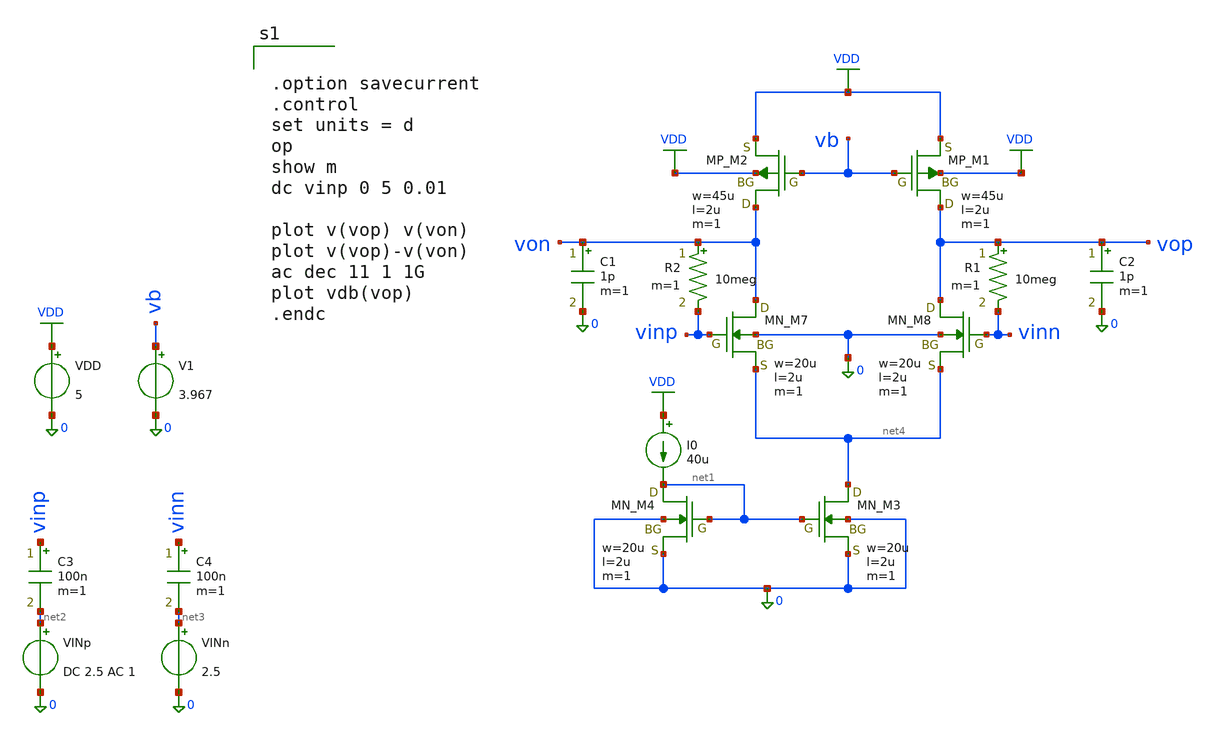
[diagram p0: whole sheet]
** sch_path: member_project/JJY_Receiver/Masahiro/jjy_recv/diff_amp/diff_amp_nin.sch
**.subckt diff_amp_nin
VDD VDD 0 5
VINp net2 0 DC 2.5 AC 1
I0 VDD net1 40u
C1 von 0 1p m=1
V1 vb 0 3.967
XM1 vop vb VDD VDD PMOS w=45u l=2u as=0 ad=0 ps=0 pd=0 nrd=0 nrs=0 m=1
XM2 von vb VDD VDD PMOS w=45u l=2u as=0 ad=0 ps=0 pd=0 nrd=0 nrs=0 m=1
XM3 net4 net1 0 0 NMOS w=20u l=2u as=0 ad=0 ps=0 pd=0 nrd=0 nrs=0 m=1
XM4 net1 net1 0 0 NMOS w=20u l=2u as=0 ad=0 ps=0 pd=0 nrd=0 nrs=0 m=1
C2 vop 0 1p m=1
VINn net3 0 2.5
XM7 von vinp net4 0 NMOS w=20u l=2u as=0 ad=0 ps=0 pd=0 nrd=0 nrs=0 m=1
XM8 vop vinn net4 0 NMOS w=20u l=2u as=0 ad=0 ps=0 pd=0 nrd=0 nrs=0 m=1
C3 vinp net2 100n m=1
C4 vinn net3 100n m=1
R1 vop vinn 10meg m=1
R2 von vinp 10meg m=1
**** begin user architecture code
 .include $::LIB/ip62_models


.option savecurrent
.control
set units = d
op
show m
dc vinp 0 5 0.01

plot v(vop) v(von)
plot v(vop)-v(von)
ac dec 11 1 1G
plot vdb(vop)
.endc


**** end user architecture code
**.ends
.GLOBAL VDD
.end
